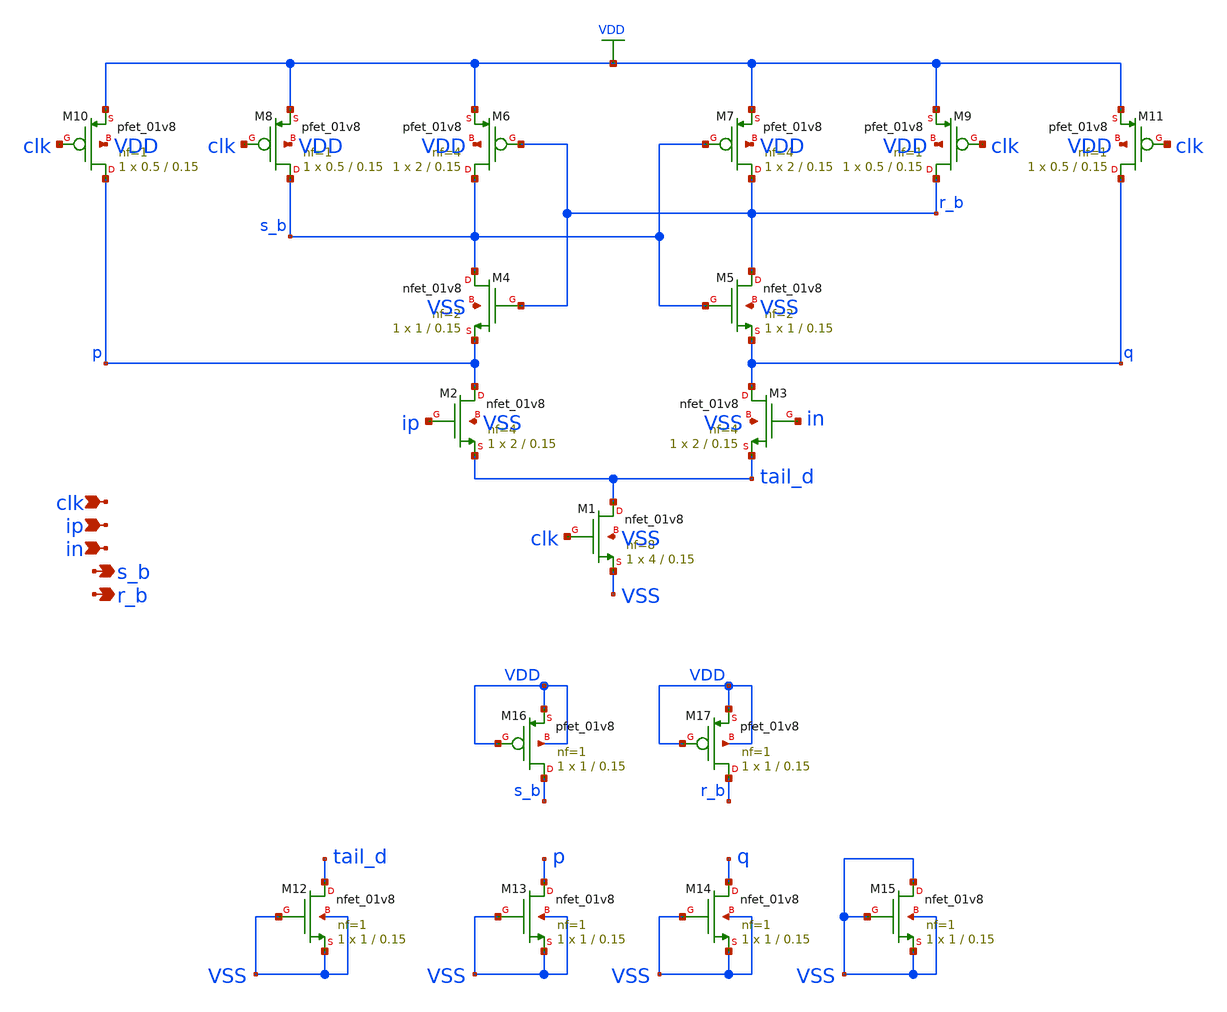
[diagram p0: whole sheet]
** sch_path: design/analog_modulator/schematic/comparator_core_small.sch
**.subckt comparator_core_small clk ip in s_b r_b
*.ipin clk
*.ipin ip
*.ipin in
*.opin s_b
*.opin r_b
XM1 tail_d clk VSS VSS sky130_fd_pr__nfet_01v8 L=0.15 W=4 nf=8 ad='int((nf+1)/2) * W/nf * 0.29' as='int((nf+2)/2) * W/nf * 0.29'
+ pd='2*int((nf+1)/2) * (W/nf + 0.29)' ps='2*int((nf+2)/2) * (W/nf + 0.29)' nrd='0.29 / W' nrs='0.29 / W'
+ sa=0 sb=0 sd=0 mult=1 m=1
XM2 p ip tail_d VSS sky130_fd_pr__nfet_01v8 L=0.15 W=2 nf=4 ad='int((nf+1)/2) * W/nf * 0.29' as='int((nf+2)/2) * W/nf * 0.29'
+ pd='2*int((nf+1)/2) * (W/nf + 0.29)' ps='2*int((nf+2)/2) * (W/nf + 0.29)' nrd='0.29 / W' nrs='0.29 / W'
+ sa=0 sb=0 sd=0 mult=1 m=1
XM3 q in tail_d VSS sky130_fd_pr__nfet_01v8 L=0.15 W=2 nf=4 ad='int((nf+1)/2) * W/nf * 0.29' as='int((nf+2)/2) * W/nf * 0.29'
+ pd='2*int((nf+1)/2) * (W/nf + 0.29)' ps='2*int((nf+2)/2) * (W/nf + 0.29)' nrd='0.29 / W' nrs='0.29 / W'
+ sa=0 sb=0 sd=0 mult=1 m=1
XM4 s_b r_b p VSS sky130_fd_pr__nfet_01v8 L=0.15 W=1 nf=2 ad='int((nf+1)/2) * W/nf * 0.29' as='int((nf+2)/2) * W/nf * 0.29'
+ pd='2*int((nf+1)/2) * (W/nf + 0.29)' ps='2*int((nf+2)/2) * (W/nf + 0.29)' nrd='0.29 / W' nrs='0.29 / W'
+ sa=0 sb=0 sd=0 mult=1 m=1
XM5 r_b s_b q VSS sky130_fd_pr__nfet_01v8 L=0.15 W=1 nf=2 ad='int((nf+1)/2) * W/nf * 0.29' as='int((nf+2)/2) * W/nf * 0.29'
+ pd='2*int((nf+1)/2) * (W/nf + 0.29)' ps='2*int((nf+2)/2) * (W/nf + 0.29)' nrd='0.29 / W' nrs='0.29 / W'
+ sa=0 sb=0 sd=0 mult=1 m=1
XM6 s_b r_b VDD VDD sky130_fd_pr__pfet_01v8 L=0.15 W=2 nf=4 ad='int((nf+1)/2) * W/nf * 0.29' as='int((nf+2)/2) * W/nf * 0.29'
+ pd='2*int((nf+1)/2) * (W/nf + 0.29)' ps='2*int((nf+2)/2) * (W/nf + 0.29)' nrd='0.29 / W' nrs='0.29 / W'
+ sa=0 sb=0 sd=0 mult=1 m=1
XM7 r_b s_b VDD VDD sky130_fd_pr__pfet_01v8 L=0.15 W=2 nf=4 ad='int((nf+1)/2) * W/nf * 0.29' as='int((nf+2)/2) * W/nf * 0.29'
+ pd='2*int((nf+1)/2) * (W/nf + 0.29)' ps='2*int((nf+2)/2) * (W/nf + 0.29)' nrd='0.29 / W' nrs='0.29 / W'
+ sa=0 sb=0 sd=0 mult=1 m=1
XM8 s_b clk VDD VDD sky130_fd_pr__pfet_01v8 L=0.15 W=0.5 nf=1 ad='int((nf+1)/2) * W/nf * 0.29' as='int((nf+2)/2) * W/nf * 0.29'
+ pd='2*int((nf+1)/2) * (W/nf + 0.29)' ps='2*int((nf+2)/2) * (W/nf + 0.29)' nrd='0.29 / W' nrs='0.29 / W'
+ sa=0 sb=0 sd=0 mult=1 m=1
XM9 r_b clk VDD VDD sky130_fd_pr__pfet_01v8 L=0.15 W=0.5 nf=1 ad='int((nf+1)/2) * W/nf * 0.29' as='int((nf+2)/2) * W/nf * 0.29'
+ pd='2*int((nf+1)/2) * (W/nf + 0.29)' ps='2*int((nf+2)/2) * (W/nf + 0.29)' nrd='0.29 / W' nrs='0.29 / W'
+ sa=0 sb=0 sd=0 mult=1 m=1
XM10 p clk VDD VDD sky130_fd_pr__pfet_01v8 L=0.15 W=0.5 nf=1 ad='int((nf+1)/2) * W/nf * 0.29' as='int((nf+2)/2) * W/nf * 0.29'
+ pd='2*int((nf+1)/2) * (W/nf + 0.29)' ps='2*int((nf+2)/2) * (W/nf + 0.29)' nrd='0.29 / W' nrs='0.29 / W'
+ sa=0 sb=0 sd=0 mult=1 m=1
XM11 q clk VDD VDD sky130_fd_pr__pfet_01v8 L=0.15 W=0.5 nf=1 ad='int((nf+1)/2) * W/nf * 0.29' as='int((nf+2)/2) * W/nf * 0.29'
+ pd='2*int((nf+1)/2) * (W/nf + 0.29)' ps='2*int((nf+2)/2) * (W/nf + 0.29)' nrd='0.29 / W' nrs='0.29 / W'
+ sa=0 sb=0 sd=0 mult=1 m=1
XM12 tail_d VSS VSS VSS sky130_fd_pr__nfet_01v8 L=0.15 W=1 nf=1 ad='int((nf+1)/2) * W/nf * 0.29' as='int((nf+2)/2) * W/nf * 0.29'
+ pd='2*int((nf+1)/2) * (W/nf + 0.29)' ps='2*int((nf+2)/2) * (W/nf + 0.29)' nrd='0.29 / W' nrs='0.29 / W'
+ sa=0 sb=0 sd=0 mult=1 m=1
XM13 p VSS VSS VSS sky130_fd_pr__nfet_01v8 L=0.15 W=1 nf=1 ad='int((nf+1)/2) * W/nf * 0.29' as='int((nf+2)/2) * W/nf * 0.29'
+ pd='2*int((nf+1)/2) * (W/nf + 0.29)' ps='2*int((nf+2)/2) * (W/nf + 0.29)' nrd='0.29 / W' nrs='0.29 / W'
+ sa=0 sb=0 sd=0 mult=1 m=1
XM14 q VSS VSS VSS sky130_fd_pr__nfet_01v8 L=0.15 W=1 nf=1 ad='int((nf+1)/2) * W/nf * 0.29' as='int((nf+2)/2) * W/nf * 0.29'
+ pd='2*int((nf+1)/2) * (W/nf + 0.29)' ps='2*int((nf+2)/2) * (W/nf + 0.29)' nrd='0.29 / W' nrs='0.29 / W'
+ sa=0 sb=0 sd=0 mult=1 m=1
XM15 VSS VSS VSS VSS sky130_fd_pr__nfet_01v8 L=0.15 W=1 nf=1 ad='int((nf+1)/2) * W/nf * 0.29' as='int((nf+2)/2) * W/nf * 0.29'
+ pd='2*int((nf+1)/2) * (W/nf + 0.29)' ps='2*int((nf+2)/2) * (W/nf + 0.29)' nrd='0.29 / W' nrs='0.29 / W'
+ sa=0 sb=0 sd=0 mult=1 m=1
XM16 s_b VDD VDD VDD sky130_fd_pr__pfet_01v8 L=0.15 W=1 nf=1 ad='int((nf+1)/2) * W/nf * 0.29' as='int((nf+2)/2) * W/nf * 0.29'
+ pd='2*int((nf+1)/2) * (W/nf + 0.29)' ps='2*int((nf+2)/2) * (W/nf + 0.29)' nrd='0.29 / W' nrs='0.29 / W'
+ sa=0 sb=0 sd=0 mult=1 m=1
XM17 r_b VDD VDD VDD sky130_fd_pr__pfet_01v8 L=0.15 W=1 nf=1 ad='int((nf+1)/2) * W/nf * 0.29' as='int((nf+2)/2) * W/nf * 0.29'
+ pd='2*int((nf+1)/2) * (W/nf + 0.29)' ps='2*int((nf+2)/2) * (W/nf + 0.29)' nrd='0.29 / W' nrs='0.29 / W'
+ sa=0 sb=0 sd=0 mult=1 m=1
**.ends
.GLOBAL VDD
.end
